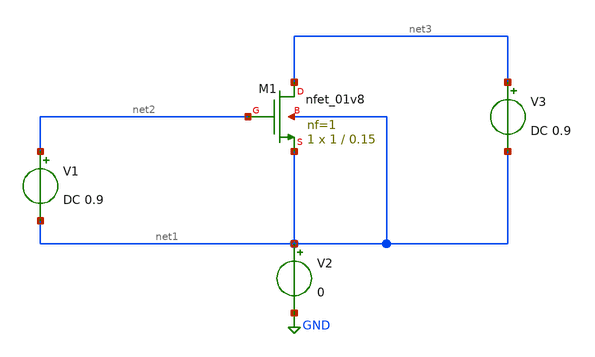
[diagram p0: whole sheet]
** sch_path: xschem/untitled-1.sch
**.subckt untitled-1
V1 net2 net1 DC 0.9
V2 net1 GND 0
V3 net3 net1 DC 0.9
XM1 net3 net2 net1 net1 sky130_fd_pr__nfet_01v8 L=0.15 W=1 nf=1 ad='int((nf+1)/2) * W/nf * 0.29' as='int((nf+2)/2) * W/nf * 0.29'
+ pd='2*int((nf+1)/2) * (W/nf + 0.29)' ps='2*int((nf+2)/2) * (W/nf + 0.29)' nrd='0.29 / W' nrs='0.29 / W'
+ sa=0 sb=0 sd=0 mult=1 m=1
**** begin user architecture code

** opencircuitdesign pdks install
.lib $::SKYWATER_MODELS/sky130.lib.spice tt
.include /usr/local/share/pdk/sky130A/libs.ref/sky130_fd_sc_hd/spice/sky130_fd_sc_hd.spice



.option wnflag=0
.option savecurrents
.control
set @m.xm1.msky130_fd_pr__nfet_01v8=nmosfet
global netlist_dir .
set wr_singlescale
save all  @m.xm1.msky130_fd_pr__nfet_01v8[vgs]  @m.xm1.msky130_fd_pr__nfet_01v8[vth]
+  @m.xm1.msky130_fd_pr__nfet_01v8[vds]  @m.xm1.msky130_fd_pr__nfet_01v8[vdsat]  @m.xm1.msky130_fd_pr__nfet_01v8[gm]
+  @m.xm1.msky130_fd_pr__nfet_01v8[gds]  @m.xm1.msky130_fd_pr__nfet_01v8[id]
op
show
showmod m.xm1.msky130_fd_pr__nfet_01v8
dc V1 0 1.8 0.01
wrdata output_nmos_${current_length}.txt  @m.xm1.msky130_fd_pr__nfet_01v8[vgs]  @m.xm1.msky130_fd_pr__nfet_01v8[vth]
+  @m.xm1.msky130_fd_pr__nfet_01v8[vds]  @m.xm1.msky130_fd_pr__nfet_01v8[vdsat]  @m.xm1.msky130_fd_pr__nfet_01v8[gm]
+  @m.xm1.msky130_fd_pr__nfet_01v8[gds]  @m.xm1.msky130_fd_pr__nfet_01v8[id]

** plot data
plot @m.xm1.msky130_fd_pr__nfet_01v8[gm]/@m.xm1.msky130_fd_pr__nfet_01v8[id] vs
+ @m.xm1.msky130_fd_pr__nfet_01v8[vds]
plot @m.xm1.msky130_fd_pr__nfet_01v8[gm]/@m.xm1.msky130_fd_pr__nfet_01v8[gds] vs
+ @m.xm1.msky130_fd_pr__nfet_01v8[gm]/@m.xm1.msky130_fd_pr__nfet_01v8[id]
plot TEMP
.endc

**** end user architecture code
**.ends
.GLOBAL GND
.end
